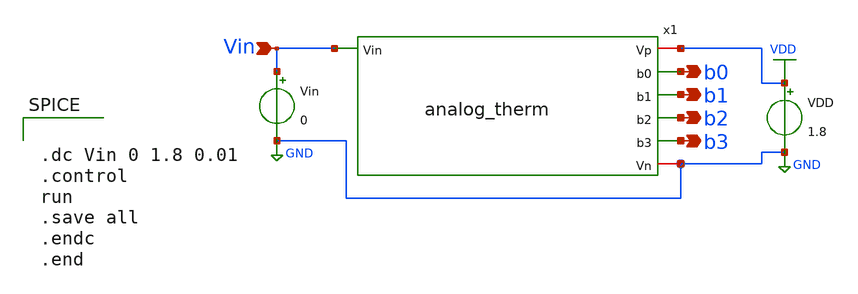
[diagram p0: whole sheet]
** sch_path: xschem/Vth_sch/Pre_layout/analog_therm.sch
**.subckt analog_therm b0 b1 b2 b3 Vin
*.opin b0
*.opin b1
*.opin b2
*.opin b3
*.ipin Vin
VDD VDD GND 1.8
Vin Vin GND 0
x1 VDD Vin b0 b1 b2 b3 GND analog_therm
**** begin user architecture code


.dc Vin 0 1.8 0.01
.control
run
.save all
.endc
.end


 .lib $::SKYWATER_MODELS/sky130.lib.spice tt
.include $::SKYWATER_STDCELLS/sky130_fd_sc_hd.spice

**** end user architecture code
**.ends
.GLOBAL VDD
.GLOBAL GND
.end
